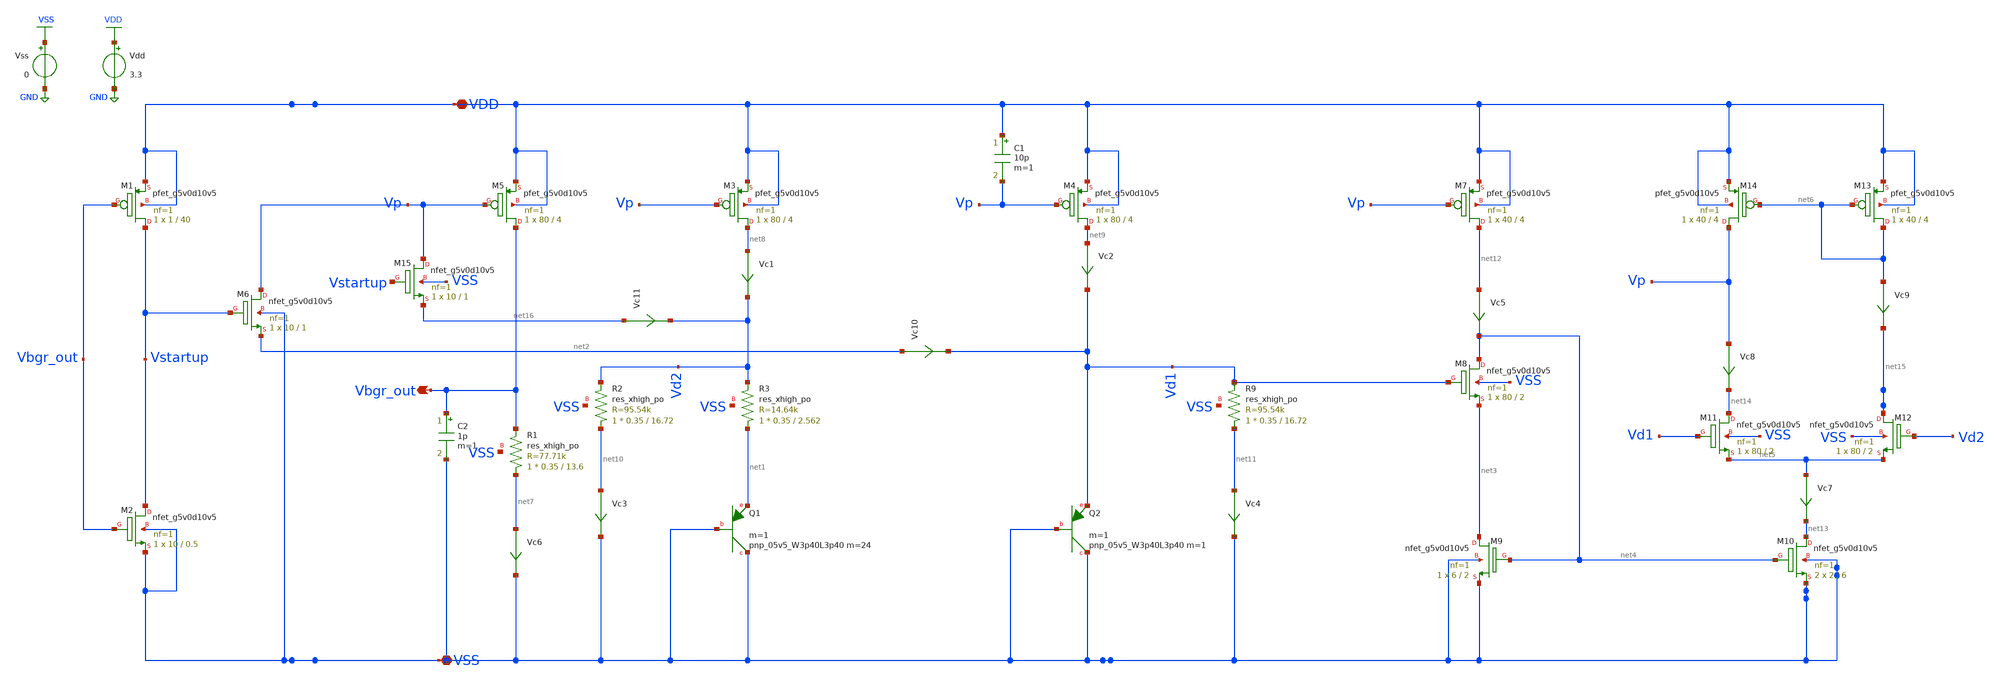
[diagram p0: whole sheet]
** sch_path: Schematic/bgr_1.sch
**.subckt bgr_1 VDD VSS Vbgr_out
*.iopin VDD
*.iopin VSS
*.opin Vbgr_out
XM1 Vstartup Vbgr_out VDD VDD sky130_fd_pr__pfet_g5v0d10v5 L=40 W=1 nf=1 ad='int((nf+1)/2) * W/nf * 0.29'
+ as='int((nf+2)/2) * W/nf * 0.29' pd='2*int((nf+1)/2) * (W/nf + 0.29)' ps='2*int((nf+2)/2) * (W/nf + 0.29)'
+ nrd='0.29 / W' nrs='0.29 / W' sa=0 sb=0 sd=0 mult=1 m=1
XM2 Vstartup Vbgr_out VSS VSS sky130_fd_pr__nfet_g5v0d10v5 L=0.5 W=10 nf=1 ad='int((nf+1)/2) * W/nf * 0.29'
+ as='int((nf+2)/2) * W/nf * 0.29' pd='2*int((nf+1)/2) * (W/nf + 0.29)' ps='2*int((nf+2)/2) * (W/nf + 0.29)'
+ nrd='0.29 / W' nrs='0.29 / W' sa=0 sb=0 sd=0 mult=1 m=1
XM3 net8 Vp VDD VDD sky130_fd_pr__pfet_g5v0d10v5 L=4 W=80 nf=1 ad='int((nf+1)/2) * W/nf * 0.29' as='int((nf+2)/2) * W/nf * 0.29'
+ pd='2*int((nf+1)/2) * (W/nf + 0.29)' ps='2*int((nf+2)/2) * (W/nf + 0.29)' nrd='0.29 / W' nrs='0.29 / W'
+ sa=0 sb=0 sd=0 mult=1 m=1
XQ1 VSS VSS net1 sky130_fd_pr__pnp_05v5_W3p40L3p40 m=24 m=1
XM4 net9 Vp VDD VDD sky130_fd_pr__pfet_g5v0d10v5 L=4 W=80 nf=1 ad='int((nf+1)/2) * W/nf * 0.29' as='int((nf+2)/2) * W/nf * 0.29'
+ pd='2*int((nf+1)/2) * (W/nf + 0.29)' ps='2*int((nf+2)/2) * (W/nf + 0.29)' nrd='0.29 / W' nrs='0.29 / W'
+ sa=0 sb=0 sd=0 mult=1 m=1
XQ2 VSS VSS Vd1 sky130_fd_pr__pnp_05v5_W3p40L3p40 m=1 m=1
XM5 Vbgr_out Vp VDD VDD sky130_fd_pr__pfet_g5v0d10v5 L=4 W=80 nf=1 ad='int((nf+1)/2) * W/nf * 0.29' as='int((nf+2)/2) * W/nf * 0.29'
+ pd='2*int((nf+1)/2) * (W/nf + 0.29)' ps='2*int((nf+2)/2) * (W/nf + 0.29)' nrd='0.29 / W' nrs='0.29 / W'
+ sa=0 sb=0 sd=0 mult=1 m=1
XM6 Vp Vstartup net2 VSS sky130_fd_pr__nfet_g5v0d10v5 L=1 W=10 nf=1 ad='int((nf+1)/2) * W/nf * 0.29'
+ as='int((nf+2)/2) * W/nf * 0.29' pd='2*int((nf+1)/2) * (W/nf + 0.29)' ps='2*int((nf+2)/2) * (W/nf + 0.29)'
+ nrd='0.29 / W' nrs='0.29 / W' sa=0 sb=0 sd=0 mult=1 m=1
Vss VSS GND 0
Vdd VDD GND 3.3
XM7 net12 Vp VDD VDD sky130_fd_pr__pfet_g5v0d10v5 L=4 W=40 nf=1 ad='int((nf+1)/2) * W/nf * 0.29' as='int((nf+2)/2) * W/nf * 0.29'
+ pd='2*int((nf+1)/2) * (W/nf + 0.29)' ps='2*int((nf+2)/2) * (W/nf + 0.29)' nrd='0.29 / W' nrs='0.29 / W'
+ sa=0 sb=0 sd=0 mult=1 m=1
XM8 net4 Vd1 net3 VSS sky130_fd_pr__nfet_g5v0d10v5 L=2 W=80 nf=1 ad='int((nf+1)/2) * W/nf * 0.29' as='int((nf+2)/2) * W/nf * 0.29'
+ pd='2*int((nf+1)/2) * (W/nf + 0.29)' ps='2*int((nf+2)/2) * (W/nf + 0.29)' nrd='0.29 / W' nrs='0.29 / W'
+ sa=0 sb=0 sd=0 mult=1 m=1
XM9 net3 net4 VSS VSS sky130_fd_pr__nfet_g5v0d10v5 L=2 W=6 nf=1 ad='int((nf+1)/2) * W/nf * 0.29' as='int((nf+2)/2) * W/nf * 0.29'
+ pd='2*int((nf+1)/2) * (W/nf + 0.29)' ps='2*int((nf+2)/2) * (W/nf + 0.29)' nrd='0.29 / W' nrs='0.29 / W'
+ sa=0 sb=0 sd=0 mult=1 m=1
XM10 net13 net4 VSS VSS sky130_fd_pr__nfet_g5v0d10v5 L=6 W=2 nf=1 ad='int((nf+1)/2) * W/nf * 0.29' as='int((nf+2)/2) * W/nf * 0.29'
+ pd='2*int((nf+1)/2) * (W/nf + 0.29)' ps='2*int((nf+2)/2) * (W/nf + 0.29)' nrd='0.29 / W' nrs='0.29 / W'
+ sa=0 sb=0 sd=0 mult=2 m=2
XM11 net14 Vd1 net5 VSS sky130_fd_pr__nfet_g5v0d10v5 L=2 W=80 nf=1 ad='int((nf+1)/2) * W/nf * 0.29' as='int((nf+2)/2) * W/nf * 0.29'
+ pd='2*int((nf+1)/2) * (W/nf + 0.29)' ps='2*int((nf+2)/2) * (W/nf + 0.29)' nrd='0.29 / W' nrs='0.29 / W'
+ sa=0 sb=0 sd=0 mult=1 m=1
XM12 net15 Vd2 net5 VSS sky130_fd_pr__nfet_g5v0d10v5 L=2 W=80 nf=1 ad='int((nf+1)/2) * W/nf * 0.29' as='int((nf+2)/2) * W/nf * 0.29'
+ pd='2*int((nf+1)/2) * (W/nf + 0.29)' ps='2*int((nf+2)/2) * (W/nf + 0.29)' nrd='0.29 / W' nrs='0.29 / W'
+ sa=0 sb=0 sd=0 mult=1 m=1
XM13 net6 net6 VDD VDD sky130_fd_pr__pfet_g5v0d10v5 L=4 W=40 nf=1 ad='int((nf+1)/2) * W/nf * 0.29' as='int((nf+2)/2) * W/nf * 0.29'
+ pd='2*int((nf+1)/2) * (W/nf + 0.29)' ps='2*int((nf+2)/2) * (W/nf + 0.29)' nrd='0.29 / W' nrs='0.29 / W'
+ sa=0 sb=0 sd=0 mult=1 m=1
XM14 Vp net6 VDD VDD sky130_fd_pr__pfet_g5v0d10v5 L=4 W=40 nf=1 ad='int((nf+1)/2) * W/nf * 0.29' as='int((nf+2)/2) * W/nf * 0.29'
+ pd='2*int((nf+1)/2) * (W/nf + 0.29)' ps='2*int((nf+2)/2) * (W/nf + 0.29)' nrd='0.29 / W' nrs='0.29 / W'
+ sa=0 sb=0 sd=0 mult=1 m=1
Vc6 net7 VSS 0
.save i(vc6)
Vc1 net8 Vd2 0
.save i(vc1)
Vc2 net9 Vd1 0
.save i(vc2)
Vc3 net10 VSS 0
.save i(vc3)
Vc4 net11 VSS 0
.save i(vc4)
Vc5 net12 net4 0
.save i(vc5)
Vc7 net5 net13 0
.save i(vc7)
Vc8 Vp net14 0
.save i(vc8)
Vc9 net6 net15 0
.save i(vc9)
Vc10 net2 Vd1 0
.save i(vc10)
C1 VDD Vp 10p m=1
C2 Vbgr_out VSS 1p m=1
XR9 net11 Vd1 VSS sky130_fd_pr__res_xhigh_po W=0.35 L=16.72 mult=1 m=1
XR2 net10 Vd2 VSS sky130_fd_pr__res_xhigh_po W=0.35 L=16.72 mult=1 m=1
XR3 net1 Vd2 VSS sky130_fd_pr__res_xhigh_po W=0.35 L=2.562 mult=1 m=1
XR1 net7 Vbgr_out VSS sky130_fd_pr__res_xhigh_po W=0.35 L=13.6 mult=1 m=1
XM15 Vp Vstartup net16 VSS sky130_fd_pr__nfet_g5v0d10v5 L=1 W=10 nf=1 ad='int((nf+1)/2) * W/nf * 0.29'
+ as='int((nf+2)/2) * W/nf * 0.29' pd='2*int((nf+1)/2) * (W/nf + 0.29)' ps='2*int((nf+2)/2) * (W/nf + 0.29)'
+ nrd='0.29 / W' nrs='0.29 / W' sa=0 sb=0 sd=0 mult=1 m=1
Vc11 net16 Vd2 0
.save i(vc11)
**** begin user architecture code
** manual skywater pdks install (with patches applied)
* .lib $::SKYWATER_MODELS/models/sky130.lib.spice tt

** opencircuitdesign pdks install
.lib $::SKYWATER_MODELS/sky130.lib.spice tt
.include $::SKYWATER_STDCELLS/sky130_fd_sc_hd.spice

**** end user architecture code
**.ends
.GLOBAL VSS
.GLOBAL GND
.GLOBAL VDD
**** begin user architecture code


.option METHOD=GEAR CHGTOL=1e-15 TRTOL=1 RELTOL=0.0001 VNTOL=0.1u
.option savecurrents savevoltages
.control
save all
//set temp=125
//op
//dc temp -40 125 10
dc Vdd 0 3.3 0.01
//tran 100n 10u
save v(Vdd) v(vbgr_out)
plot v(vbgr_out) V(Vdd)
print v(Vbgr_out)
//save all
write  /home/vaibhav/sky130-example/bgr_1.raw
.endc


**** end user architecture code
.end
